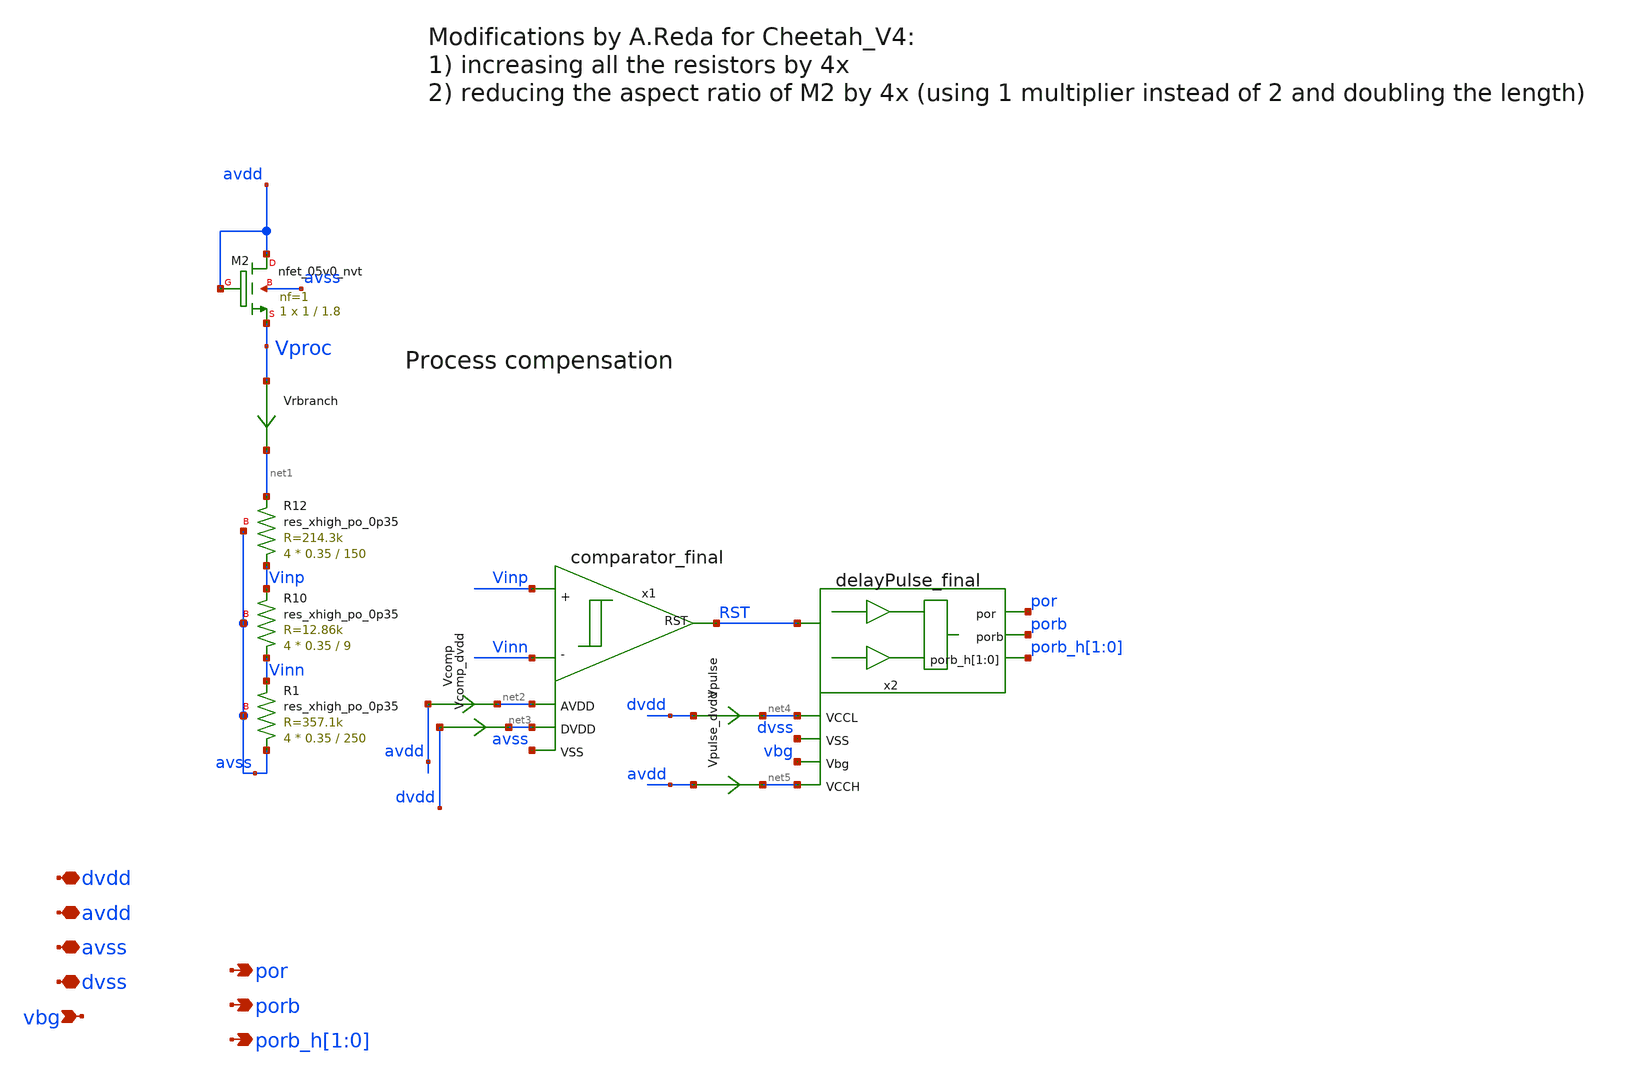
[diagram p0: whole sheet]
** sch_path: xschem/sky130_sw_ip__bgrref_por.sch
**.subckt sky130_sw_ip__bgrref_por avdd por avss dvdd porb vbg porb_h[1],porb_h[0] dvss
*.iopin avdd
*.opin por
*.iopin avss
*.iopin dvdd
*.opin porb
*.ipin vbg
*.opin porb_h[1],porb_h[0]
*.iopin dvss
x1 Vinn Vinp RST avss net2 net3 comparator_final
XR1 avss Vinn avss sky130_fd_pr__res_xhigh_po_0p35 L=250 mult=4 m=4
XR10 Vinn Vinp avss sky130_fd_pr__res_xhigh_po_0p35 L=9 mult=4 m=4
XR12 Vinp net1 avss sky130_fd_pr__res_xhigh_po_0p35 L=150 mult=4 m=4
x2 RST por net4 dvss vbg net5 porb porb_h[1] porb_h[0] delayPulse_final
XM2 avdd avdd Vproc avss sky130_fd_pr__nfet_05v0_nvt L=1.8 W=1 nf=1 ad='int((nf+1)/2) * W/nf * 0.29'
+ as='int((nf+2)/2) * W/nf * 0.29' pd='2*int((nf+1)/2) * (W/nf + 0.29)' ps='2*int((nf+2)/2) * (W/nf + 0.29)'
+ nrd='0.29 / W' nrs='0.29 / W' sa=0 sb=0 sd=0 mult=1 m=1
Vrbranch Vproc net1 0
.save i(vrbranch)
Vcomp avdd net2 0
.save i(vcomp)
Vcomp_dvdd dvdd net3 0
.save i(vcomp_dvdd)
Vpulse dvdd net4 0
.save i(vpulse)
Vpulse_dvdd avdd net5 0
.save i(vpulse_dvdd)
**.ends
.end
